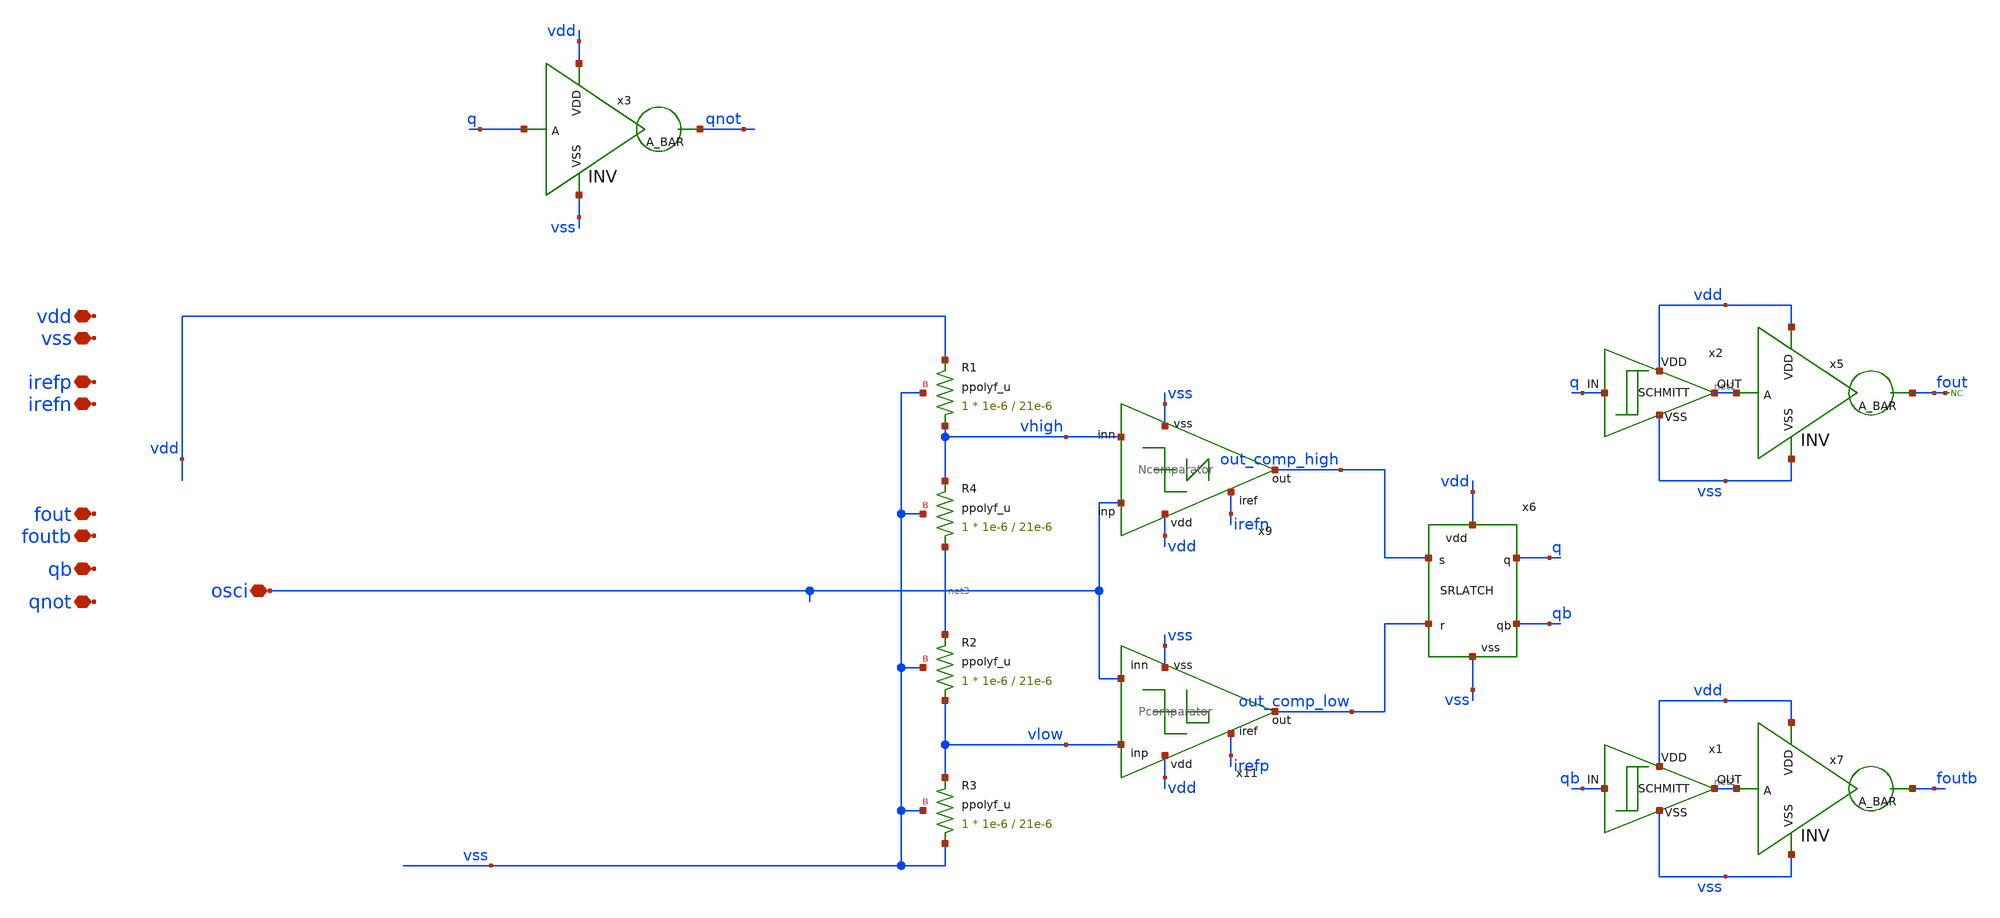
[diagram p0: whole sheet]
** sch_path: designs/libs/qw_core_analog/VCOfinal_noCP/VCOfinal_noCP.sch
**.subckt VCOfinal_noCP osci vdd vss irefp irefn fout foutb qb qnot
*.iopin osci
*.iopin vdd
*.iopin vss
*.iopin irefp
*.iopin irefn
*.iopin fout
*.iopin foutb
*.iopin qb
*.iopin qnot
x3 vdd q qnot vss INV
x5 vdd net1 fout vss INV
x7 vdd net2 foutb vss INV
* noconn fout
XR3 vss vlow vss ppolyf_u r_width=1e-6 r_length=21e-6 m=1
XR1 vhigh vdd vss ppolyf_u r_width=1e-6 r_length=21e-6 m=1
XR2 vlow net3 vss ppolyf_u r_width=1e-6 r_length=21e-6 m=1
XR4 net3 vhigh vss ppolyf_u r_width=1e-6 r_length=21e-6 m=1
x6 vdd out_comp_high q qb out_comp_low vss SRLATCH
x9 vdd osci out_comp_high vhigh irefn vss Ncomparator
x11 vdd irefp vlow out_comp_low osci vss Pcomparator
x2 q net1 vdd vss SCHMITT
x1 qb net2 vdd vss SCHMITT
**.ends
.end
